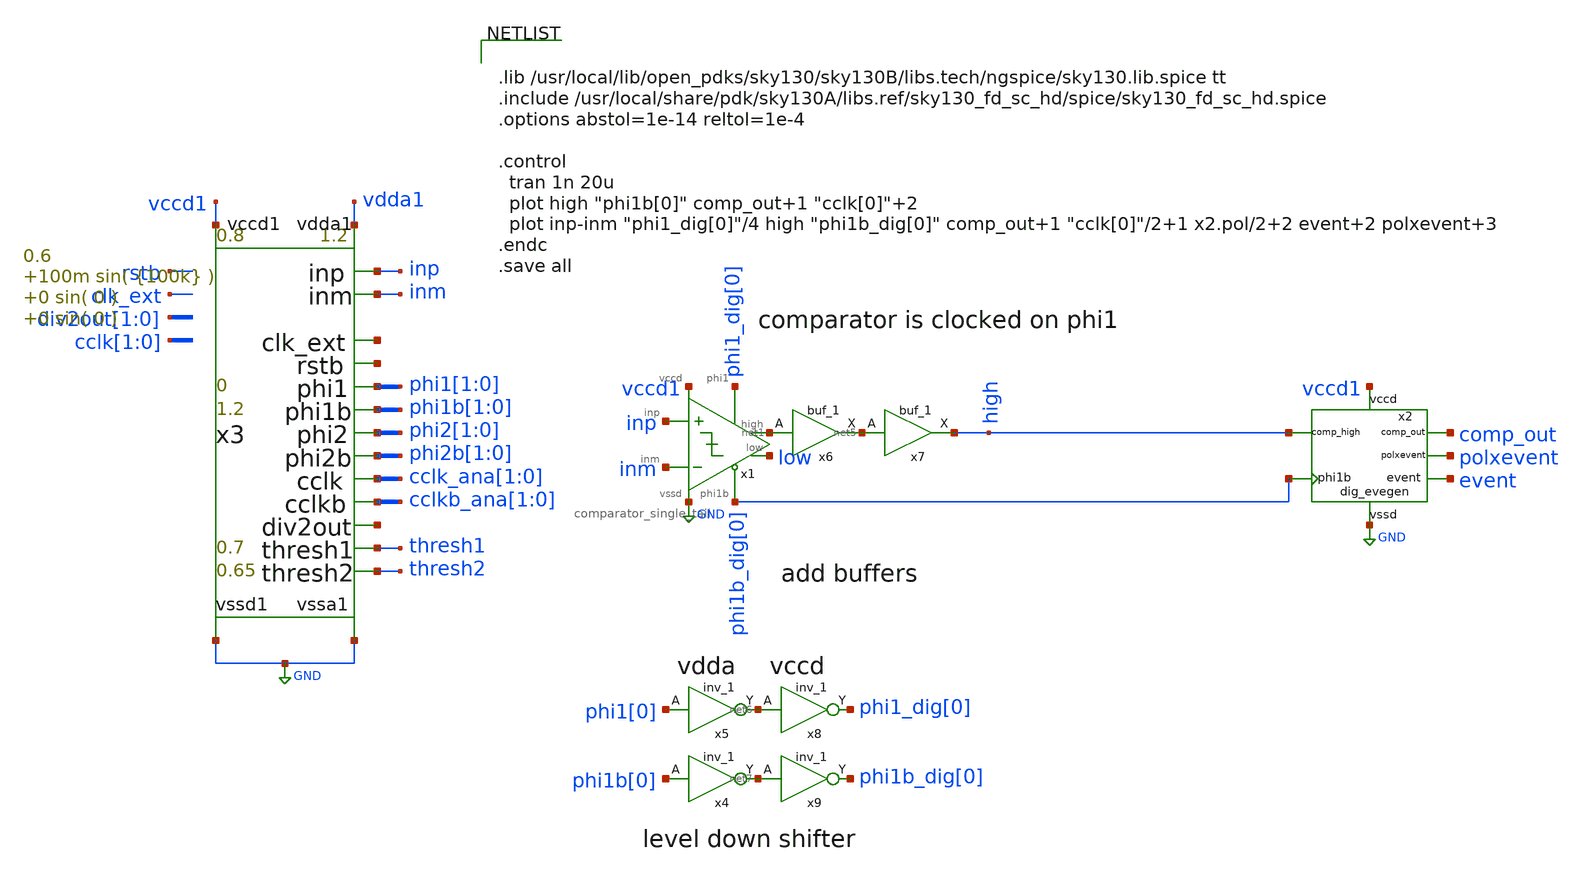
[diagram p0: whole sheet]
** sch_path: xschem/test_bench/comparator_pol_event_tb.sch
**.subckt comparator_pol_event_tb
x1 inp inm net1 phi1_dig[0] phi1b_dig[0] low vccd1 GND comparator_single_tail Wplus=0.42 Lplus=0.42
+ Wminus=0.42 Lminus=0.15
x3 thresh1 thresh2 vdda1 GND inp inm net2 net3 vccd1 GND phi1[1] phi1b[1] phi2[1] phi2b[1] cclk_ana[1]
+ cclkb_ana[1] net4 risc_signals p_vdda1=1.2 p_vccd1=0.8 p_fclk={256*10k} p_duty_cycle=0.5 p_rstb_delay={1.5/p_fclk}
+ p_rstb_tr=5n p_thresh1=0.7 p_thresh2=0.65 p_vpb=0 p_vnb=1.2 p_vcm=0.6 p_amp1=100m p_f1={100k} p_amp2=0
+ p_f2=0 p_amp3=0 p_f3=0
x6 net1 gnd gnd vccd1 vccd1 net5 sky130_fd_sc_hd__buf_1
x7 net5 gnd gnd vccd1 vccd1 high sky130_fd_sc_hd__buf_1
x2 phi1b_dig[0] event polxevent vccd1 GND high comp_out dig_evegen
x5 phi1[0] gnd gnd vdda1 vdda1 net6 sky130_fd_sc_hd__inv_1
x8 net6 gnd gnd vccd1 vccd1 phi1_dig[0] sky130_fd_sc_hd__inv_1
x4 phi1b[0] gnd gnd vdda1 vdda1 net7 sky130_fd_sc_hd__inv_1
x9 net7 gnd gnd vccd1 vccd1 phi1b_dig[0] sky130_fd_sc_hd__inv_1
**** begin user architecture code


.lib /usr/local/lib/open_pdks/sky130/sky130B/libs.tech/ngspice/sky130.lib.spice tt
.include /usr/local/share/pdk/sky130A/libs.ref/sky130_fd_sc_hd/spice/sky130_fd_sc_hd.spice
.options abstol=1e-14 reltol=1e-4

.control
  tran 1n 20u
  plot high "phi1b[0]" comp_out+1 "cclk[0]"+2
  plot inp-inm "phi1_dig[0]"/4 high "phi1b_dig[0]" comp_out+1 "cclk[0]"/2+1 x2.pol/2+2 event+2
+ polxevent+3
.endc
.save all


**** end user architecture code
**.ends
.GLOBAL GND
.end
